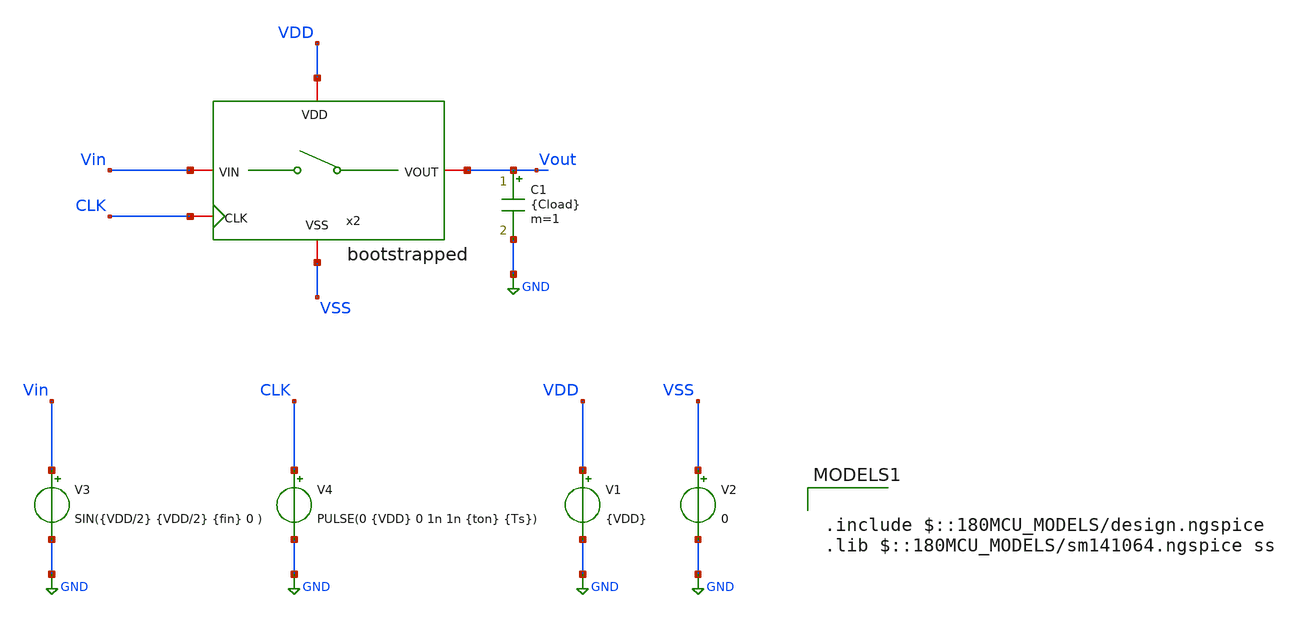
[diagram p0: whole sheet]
** sch_path: designs/sar_adc/samplehold/bootstrapped/xschem/tb_bootstrapped.sch
**.subckt tb_bootstrapped
V1 VDD GND {VDD}
V2 VSS GND 0
V3 Vin GND SIN({VDD/2} {VDD/2} {fin} 0 )
V4 CLK GND PULSE(0 {VDD} 0 1n 1n {ton} {Ts})
C1 Vout GND {Cload} m=1
x2 VDD VSS CLK Vin Vout bootstrapped
**** begin user architecture code

.include $::180MCU_MODELS/design.ngspice
.lib $::180MCU_MODELS/sm141064.ngspice ss




* Sampling clock
.param Fs = 5Meg
.param ton = Ts/12

* Input parameters
.param Ts = 1/Fs
.param Ns = 1024
.param Nc = 509
.param fin = Nc/Ns*Fs

* Test-bench parameters
.temp 27
.param VDD = 3.3
.param Cload = 1p

.save all

.control

* Local variables for .control
let Fs = 5Meg
let Ns = 1024
let Nspare = 5

let tstep = 1/(Fs*240)
let tstop = (Ns + Nspare)/Fs

* Transient simulation
tran $&tstep $&tstop

linearize v(vout) v(vin) v(clk)
wrdata tb_bootstrapped.csv v(vin) v(vout) v(clk)

plot v(vin) v(vout)
plot v(vin) v(vout) xl 0 4u

.endc



**** end user architecture code
**.ends
.GLOBAL GND
.end
